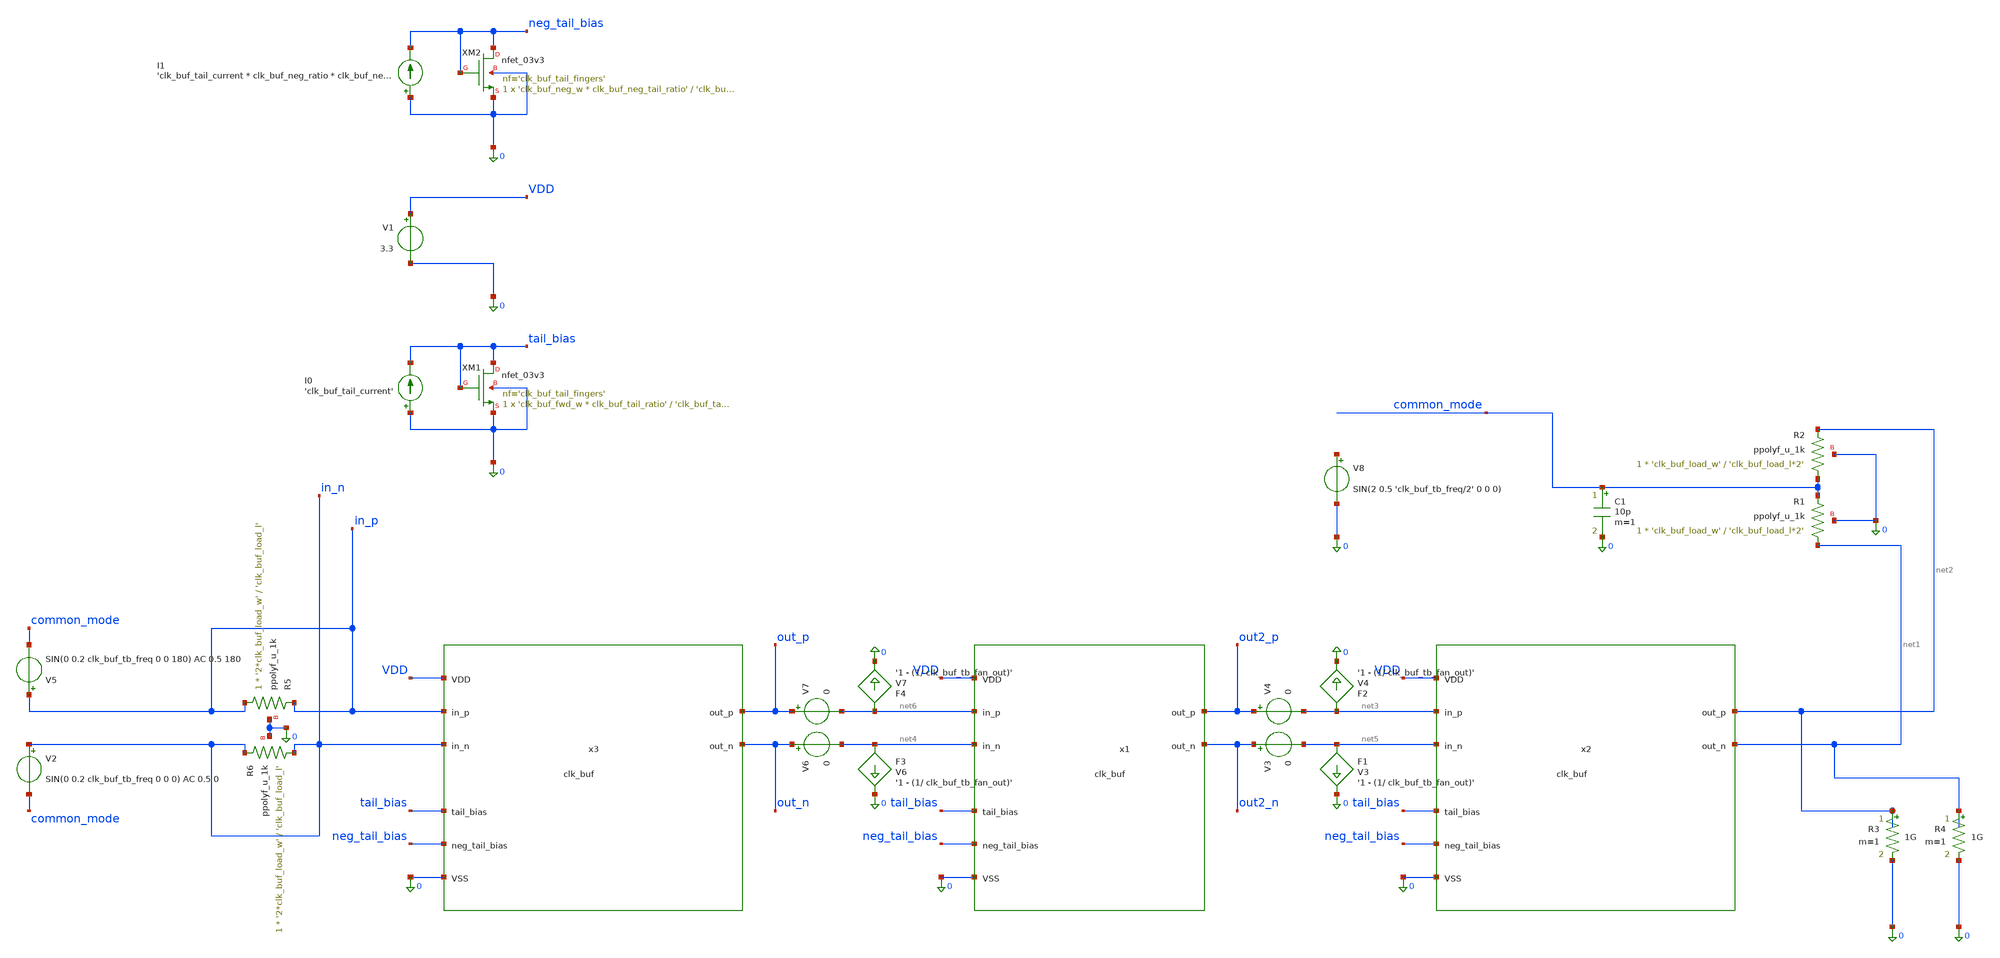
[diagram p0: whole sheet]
** sch_path: xschem/clk_buf_tb.sch
**.subckt clk_buf_tb
x1 0 VDD out2_n out2_p net6 net4 tail_bias neg_tail_bias clk_buf
XM1 tail_bias tail_bias 0 0 nfet_03v3 L='clk_buf_tail_l' W='clk_buf_fwd_w * clk_buf_tail_ratio' nf='clk_buf_tail_fingers'
+ ad='int((nf+1)/2) * W/nf * 0.18u' as='int((nf+2)/2) * W/nf * 0.18u' pd='2*int((nf+1)/2) * (W/nf + 0.18u)'
+ ps='2*int((nf+2)/2) * (W/nf + 0.18u)' nrd='0.18u / W' nrs='0.18u / W' sa=0 sb=0 sd=0 m=1
x2 0 VDD net1 net2 net3 net5 tail_bias neg_tail_bias clk_buf
V1 VDD 0 3.3
I0 0 tail_bias 'clk_buf_tail_current'
V2 in_n common_mode SIN(0 0.2 clk_buf_tb_freq 0 0 0) AC 0.5 0
R3 net2 0 1G m=1
R4 net1 0 1G m=1
F1 net5 0 V3 '1 - (1/ clk_buf_tb_fan_out)'
XR1 net1 common_mode 0 ppolyf_u_1k r_width='clk_buf_load_w' r_length='clk_buf_load_l*2' m=1
F2 net3 0 V4 '1 - (1/ clk_buf_tb_fan_out)'
V3 out2_n net5 0
V4 out2_p net3 0
V5 in_p common_mode SIN(0 0.2 clk_buf_tb_freq 0 0 180) AC 0.5 180
XR2 common_mode net2 0 ppolyf_u_1k r_width='clk_buf_load_w' r_length='clk_buf_load_l*2' m=1
C1 common_mode 0 10p m=1
x3 0 VDD out_n out_p in_p in_n tail_bias neg_tail_bias clk_buf
V6 out_n net4 0
V7 out_p net6 0
F3 net4 0 V6 '1 - (1/ clk_buf_tb_fan_out)'
F4 net6 0 V7 '1 - (1/ clk_buf_tb_fan_out)'
XR5 in_p in_p 0 ppolyf_u_1k r_width='2*clk_buf_load_w' r_length='clk_buf_load_l' m=1
XR6 in_n in_n 0 ppolyf_u_1k r_width='2*clk_buf_load_w' r_length='clk_buf_load_l' m=1
V8 net7 0 SIN(2 0.5 'clk_buf_tb_freq/2' 0 0 0)
XM2 neg_tail_bias neg_tail_bias 0 0 nfet_03v3 L='clk_buf_tail_l' W='clk_buf_neg_w * clk_buf_neg_tail_ratio'
+ nf='clk_buf_tail_fingers' ad='int((nf+1)/2) * W/nf * 0.18u' as='int((nf+2)/2) * W/nf * 0.18u' pd='2*int((nf+1)/2) * (W/nf + 0.18u)'
+ ps='2*int((nf+2)/2) * (W/nf + 0.18u)' nrd='0.18u / W' nrs='0.18u / W' sa=0 sb=0 sd=0 m=1
I1 0 neg_tail_bias 'clk_buf_tail_current * clk_buf_neg_ratio * clk_buf_neg_tail_adjust'
**** begin user architecture code
 .include $::180MCU_MODELS/design.ngspice
.lib $::180MCU_MODELS/sm141064.ngspice typical
.lib $::180MCU_MODELS/sm141064.ngspice res_typical


.option savecurrents

.param clk_buf_fwd_w=16u
.param clk_buf_fwd_fingers=2
.param clk_buf_in_out_ratio=0.55
.param clk_buf_tail_fingers=4
.param clk_buf_tail_ratio=4
.param clk_buf_tail_l=1u
.param clk_buf_load_w=2u
.param clk_buf_load_r=4k
.param clk_buf_load_l='clk_buf_load_r/1000 * clk_buf_load_w'
.param clk_buf_neg_ratio='0.155'
.param clk_buf_neg_w='clk_buf_fwd_w * clk_buf_neg_ratio'
.param clk_buf_neg_fingers=1
.param clk_buf_neg_tail_ratio=5
.param clk_buf_neg_tail_adjust=1.5
.param clk_buf_tail_current=512u

.param clk_buf_tb_fan_out=1.78039
.param clk_buf_tb_freq=2.5G

.control
save all
*tran 5p 5n
*plot in_p in_n out_p out_n x1.net1
*plot in_p in_n out_p out_n x1.net1 v(out2_p) v(out2_n) ((v(out_p) + v(out_n))/2) ((v(out2_p) +
*+ v(out2_n)) / 2)
op
write clk_buf_tb.raw
ac dec 200 100M 100G
*set units = degrees
*plot (db(v(out2_n, out2_p) - v(out_n, out_p))) (cph(v(out2_n, out2_p) - v(out_n, out_p)) *(1/2/pi *
*+ 360/ 10))
*plot (db( (v(out2_n, out2_p) - v(out_n, out_p))^5 )) (cph( (v(out2_n, out2_p) - v(out_n, out_p))^5
*+ ) *(1/2/pi * 360/ 10)) (db(v(out2_n, out2_p) - v(out_n, out_p))) (cph(v(out2_n, out2_p) - v(out_n,
*+ out_p)) *(1/2/pi * 360/ 10)) (group_delay(  (v(out2_n, out2_p) - v(out_n, out_p)) ) / (1ps ))
plot (db(v(out2_n, out2_p) - v(out_n, out_p))) (cph(v(out2_n, out2_p) - v(out_n, out_p)) *(1/2/pi *
+ 360/ 10)) (group_delay(  (v(out2_n, out2_p) - v(out_n, out_p)) ) / (10ps ))
.endc
**** end user architecture code
**.ends

* expanding   symbol:  clk_buf.sym # of pins=8
** sym_path: xschem/clk_buf.sym
** sch_path: xschem/clk_buf.sch
.subckt clk_buf VSS VDD out_n out_p in_p in_n tail_bias neg_tail_bias
*.ipin VSS
*.ipin VDD
*.opin out_n
*.opin out_p
*.ipin in_p
*.ipin in_n
*.ipin tail_bias
*.ipin neg_tail_bias
XM1 net2 in_p net1 VSS nfet_03v3 L=0.28u W='clk_buf_fwd_w * clk_buf_in_out_ratio' nf='clk_buf_fwd_fingers'
+ ad='int((nf+1)/2) * W/nf * 0.18u' as='int((nf+2)/2) * W/nf * 0.18u' pd='2*int((nf+1)/2) * (W/nf + 0.18u)'
+ ps='2*int((nf+2)/2) * (W/nf + 0.18u)' nrd='0.18u / W' nrs='0.18u / W' sa=0 sb=0 sd=0 m=1
XM3 net1 tail_bias VSS VSS nfet_03v3 L='clk_buf_tail_l' W='clk_buf_fwd_w * clk_buf_in_out_ratio * clk_buf_tail_ratio'
+ nf='clk_buf_tail_fingers' ad='int((nf+1)/2) * W/nf * 0.18u' as='int((nf+2)/2) * W/nf * 0.18u' pd='2*int((nf+1)/2) * (W/nf + 0.18u)'
+ ps='2*int((nf+2)/2) * (W/nf + 0.18u)' nrd='0.18u / W' nrs='0.18u / W' sa=0 sb=0 sd=0 m=1
XM2 net3 in_n net1 VSS nfet_03v3 L=0.28u W='clk_buf_fwd_w * clk_buf_in_out_ratio' nf='clk_buf_fwd_fingers'
+ ad='int((nf+1)/2) * W/nf * 0.18u' as='int((nf+2)/2) * W/nf * 0.18u' pd='2*int((nf+1)/2) * (W/nf + 0.18u)'
+ ps='2*int((nf+2)/2) * (W/nf + 0.18u)' nrd='0.18u / W' nrs='0.18u / W' sa=0 sb=0 sd=0 m=1
XR1 net2 VDD VSS ppolyf_u_1k r_width='clk_buf_load_w' r_length='clk_buf_load_l / clk_buf_in_out_ratio'
+ m=1
XR2 net3 VDD VSS ppolyf_u_1k r_width='clk_buf_load_w' r_length='clk_buf_load_l / clk_buf_in_out_ratio'
+ m=1
XM4 out_n net3 net4 VSS nfet_03v3 L=0.28u W='clk_buf_fwd_w' nf='clk_buf_fwd_fingers' ad='int((nf+1)/2) * W/nf * 0.18u'
+ as='int((nf+2)/2) * W/nf * 0.18u' pd='2*int((nf+1)/2) * (W/nf + 0.18u)' ps='2*int((nf+2)/2) * (W/nf + 0.18u)'
+ nrd='0.18u / W' nrs='0.18u / W' sa=0 sb=0 sd=0 m=1
XM5 net4 tail_bias VSS VSS nfet_03v3 L='clk_buf_tail_l' W='clk_buf_fwd_w * clk_buf_tail_ratio' nf='clk_buf_tail_fingers'
+ ad='int((nf+1)/2) * W/nf * 0.18u' as='int((nf+2)/2) * W/nf * 0.18u' pd='2*int((nf+1)/2) * (W/nf + 0.18u)'
+ ps='2*int((nf+2)/2) * (W/nf + 0.18u)' nrd='0.18u / W' nrs='0.18u / W' sa=0 sb=0 sd=0 m=1
XM6 out_p net2 net4 VSS nfet_03v3 L=0.28u W='clk_buf_fwd_w' nf='clk_buf_fwd_fingers' ad='int((nf+1)/2) * W/nf * 0.18u'
+ as='int((nf+2)/2) * W/nf * 0.18u' pd='2*int((nf+1)/2) * (W/nf + 0.18u)' ps='2*int((nf+2)/2) * (W/nf + 0.18u)'
+ nrd='0.18u / W' nrs='0.18u / W' sa=0 sb=0 sd=0 m=1
XR3 out_n VDD VSS ppolyf_u_1k r_width='clk_buf_load_w' r_length='clk_buf_load_l' m=1
XR4 out_p VDD VSS ppolyf_u_1k r_width='clk_buf_load_w' r_length='clk_buf_load_l' m=1
XM7 net2 out_n net5 VSS nfet_03v3 L=0.28u W='clk_buf_neg_w' nf='clk_buf_neg_fingers' ad='int((nf+1)/2) * W/nf * 0.18u'
+ as='int((nf+2)/2) * W/nf * 0.18u' pd='2*int((nf+1)/2) * (W/nf + 0.18u)' ps='2*int((nf+2)/2) * (W/nf + 0.18u)'
+ nrd='0.18u / W' nrs='0.18u / W' sa=0 sb=0 sd=0 m=1
XM8 net5 neg_tail_bias VSS VSS nfet_03v3 L='clk_buf_tail_l' W='clk_buf_neg_w * clk_buf_neg_tail_ratio'
+ nf='clk_buf_tail_fingers' ad='int((nf+1)/2) * W/nf * 0.18u' as='int((nf+2)/2) * W/nf * 0.18u' pd='2*int((nf+1)/2) * (W/nf + 0.18u)'
+ ps='2*int((nf+2)/2) * (W/nf + 0.18u)' nrd='0.18u / W' nrs='0.18u / W' sa=0 sb=0 sd=0 m=1
XM9 net3 out_p net5 VSS nfet_03v3 L=0.28u W='clk_buf_neg_w' nf='clk_buf_neg_fingers' ad='int((nf+1)/2) * W/nf * 0.18u'
+ as='int((nf+2)/2) * W/nf * 0.18u' pd='2*int((nf+1)/2) * (W/nf + 0.18u)' ps='2*int((nf+2)/2) * (W/nf + 0.18u)'
+ nrd='0.18u / W' nrs='0.18u / W' sa=0 sb=0 sd=0 m=1
.ends

.end
